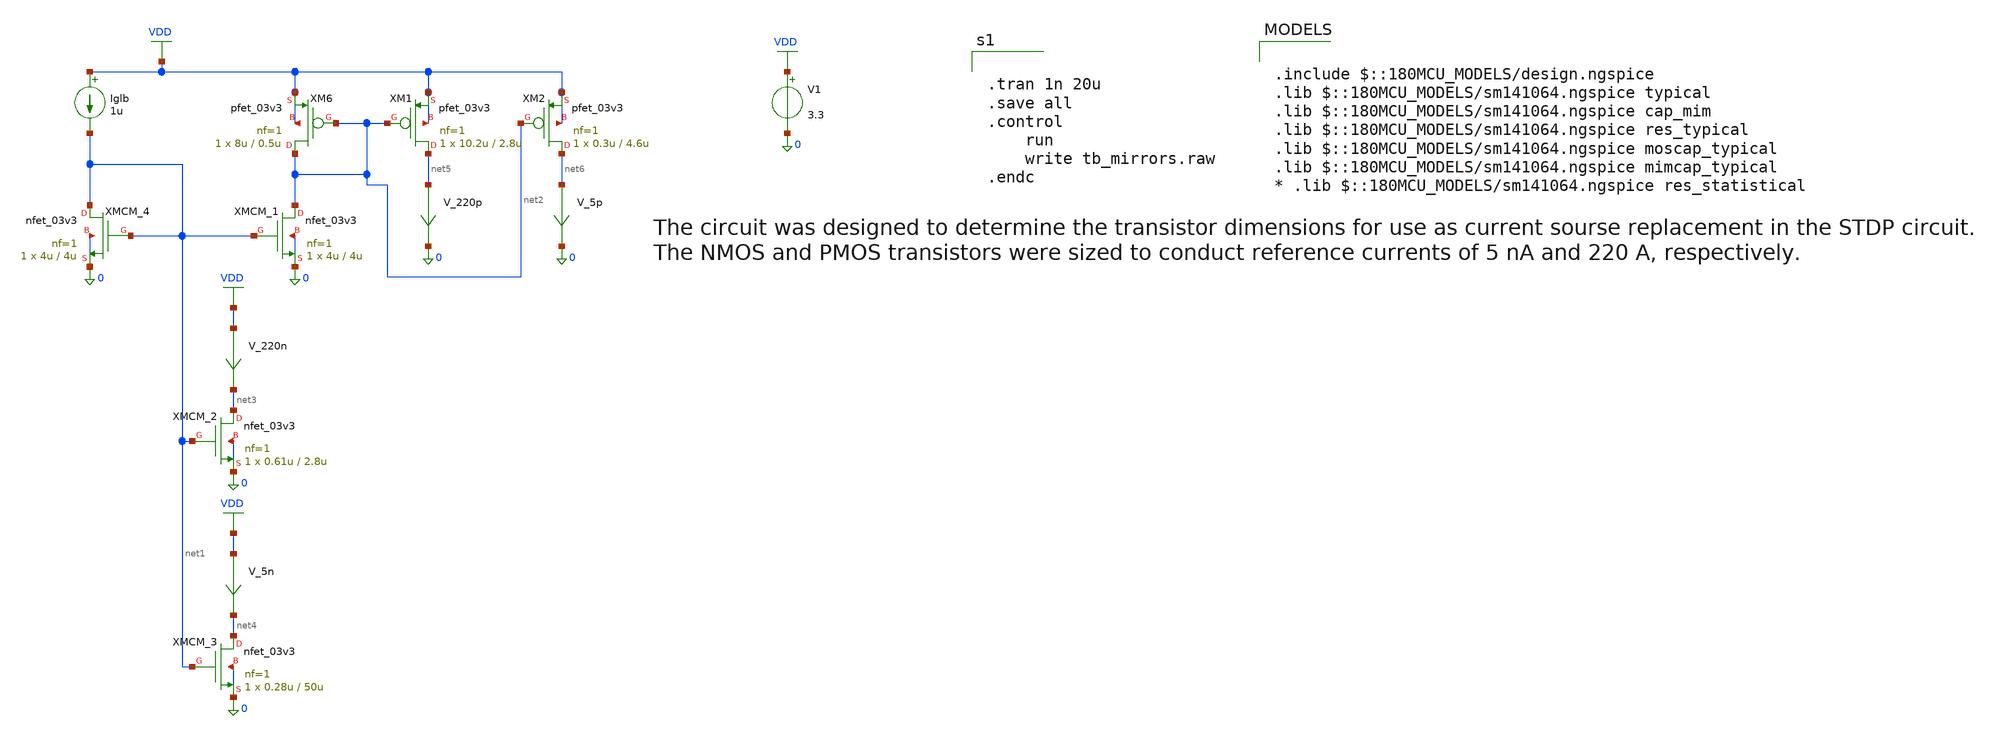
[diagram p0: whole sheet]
** sch_path: sch/stdp/tb_mirrors.sch
**.subckt tb_mirrors
XM6 net2 net2 VDD VDD pfet_03v3 L=0.5u W=8u nf=1 ad='int((nf+1)/2) * W/nf * 0.18u' as='int((nf+2)/2) * W/nf * 0.18u'
+ pd='2*int((nf+1)/2) * (W/nf + 0.18u)' ps='2*int((nf+2)/2) * (W/nf + 0.18u)' nrd='0.18u / W' nrs='0.18u / W'
+ sa=0 sb=0 sd=0 m=1
XMCM_4 net1 net1 0 0 nfet_03v3 L=4u W=4u nf=1 ad='int((nf+1)/2) * W/nf * 0.18u' as='int((nf+2)/2) * W/nf * 0.18u'
+ pd='2*int((nf+1)/2) * (W/nf + 0.18u)' ps='2*int((nf+2)/2) * (W/nf + 0.18u)' nrd='0.18u / W' nrs='0.18u / W'
+ sa=0 sb=0 sd=0 m=1
Iglb VDD net1 1u
XMCM_1 net2 net1 0 0 nfet_03v3 L=4u W=4u nf=1 ad='int((nf+1)/2) * W/nf * 0.18u' as='int((nf+2)/2) * W/nf * 0.18u'
+ pd='2*int((nf+1)/2) * (W/nf + 0.18u)' ps='2*int((nf+2)/2) * (W/nf + 0.18u)' nrd='0.18u / W' nrs='0.18u / W'
+ sa=0 sb=0 sd=0 m=1
XM1 net5 net2 VDD VDD pfet_03v3 L=2.8u W=10.2u nf=1 ad='int((nf+1)/2) * W/nf * 0.18u' as='int((nf+2)/2) * W/nf * 0.18u'
+ pd='2*int((nf+1)/2) * (W/nf + 0.18u)' ps='2*int((nf+2)/2) * (W/nf + 0.18u)' nrd='0.18u / W' nrs='0.18u / W'
+ sa=0 sb=0 sd=0 m=1
XMCM_2 net3 net1 0 0 nfet_03v3 L=2.8u W=0.61u nf=1 ad='int((nf+1)/2) * W/nf * 0.18u' as='int((nf+2)/2) * W/nf * 0.18u'
+ pd='2*int((nf+1)/2) * (W/nf + 0.18u)' ps='2*int((nf+2)/2) * (W/nf + 0.18u)' nrd='0.18u / W' nrs='0.18u / W'
+ sa=0 sb=0 sd=0 m=1
XMCM_3 net4 net1 0 0 nfet_03v3 L=50u W=0.28u nf=1 ad='int((nf+1)/2) * W/nf * 0.18u' as='int((nf+2)/2) * W/nf * 0.18u'
+ pd='2*int((nf+1)/2) * (W/nf + 0.18u)' ps='2*int((nf+2)/2) * (W/nf + 0.18u)' nrd='0.18u / W' nrs='0.18u / W'
+ sa=0 sb=0 sd=0 m=1
XM2 net6 net2 VDD VDD pfet_03v3 L=4.6u W=0.3u nf=1 ad='int((nf+1)/2) * W/nf * 0.18u' as='int((nf+2)/2) * W/nf * 0.18u'
+ pd='2*int((nf+1)/2) * (W/nf + 0.18u)' ps='2*int((nf+2)/2) * (W/nf + 0.18u)' nrd='0.18u / W' nrs='0.18u / W'
+ sa=0 sb=0 sd=0 m=1
V_220n VDD net3 0
.save i(v_220n)
V_5n VDD net4 0
.save i(v_5n)
V_220p net5 0 0
.save i(v_220p)
V_5p net6 0 0
.save i(v_5p)
V1 VDD 0 3.3
**** begin user architecture code


.tran 1n 20u
.save all
.control
	run
	write tb_mirrors.raw
.endc




.include $::180MCU_MODELS/design.ngspice
.lib $::180MCU_MODELS/sm141064.ngspice typical
.lib $::180MCU_MODELS/sm141064.ngspice cap_mim
.lib $::180MCU_MODELS/sm141064.ngspice res_typical
.lib $::180MCU_MODELS/sm141064.ngspice moscap_typical
.lib $::180MCU_MODELS/sm141064.ngspice mimcap_typical
* .lib $::180MCU_MODELS/sm141064.ngspice res_statistical

**** end user architecture code
**.ends
.GLOBAL VDD
.end
